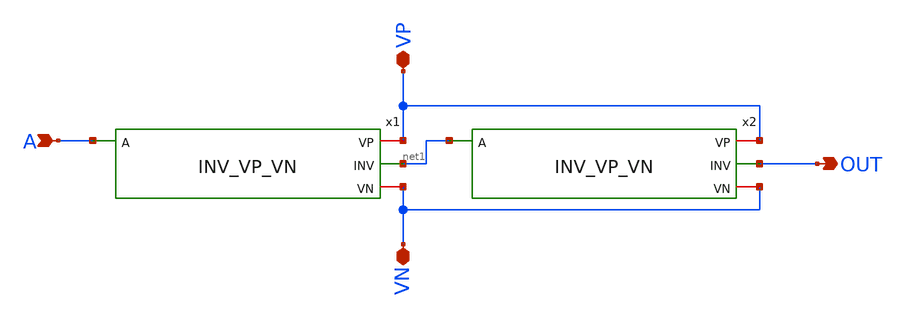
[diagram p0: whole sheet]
** sch_path: skywater_stuff/Buffer.sch
**.subckt Buffer A VP VN OUT
*.ipin A
*.iopin VP
*.iopin VN
*.opin OUT
x1 VP A net1 VN INV_VP_VN
x2 VP net1 OUT VN INV_VP_VN
**.ends
.end
